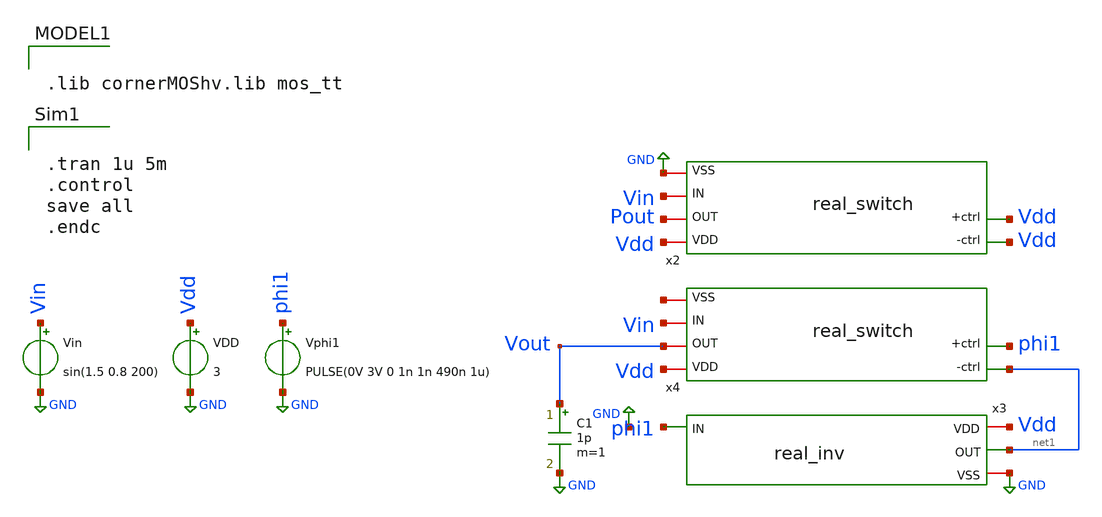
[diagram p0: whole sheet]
** sch_path: real_circuit/sandbox/TGATE_tb.sch
**.subckt TGATE_tb
VDD Vdd GND 3
Vin Vin GND sin(1.5 0.8 200)
Vphi1 phi1 GND PULSE(0V 3V 0 1n 1n 490n 1u)
x2 Vdd Vdd Pout Vin Vdd GND real_switch
x3 Vdd phi1 net1 GND real_inv
x4 net1 Vdd Vout Vin phi1 net2 real_switch
C1 Vout GND 1p m=1
**** begin user architecture code


.tran 1u 5m
.control
save all
.endc



.lib cornerMOShv.lib mos_tt

**** end user architecture code
**.ends

* expanding   symbol:  /foss/designs/real/real_switch.sym # of pins=6
** sym_path: real_circuit/sandbox/real_switch.sym
** sch_path: real_circuit/sandbox/real_switch.sch
.subckt real_switch -ctrl VDD OUT IN +ctrl VSS
*.iopin IN
*.iopin OUT
*.iopin VDD
*.iopin VSS
*.ipin +ctrl
*.ipin -ctrl
XM1 OUT -ctrl IN VSS sg13_hv_nmos w=1u l=0.6u ng=1 m=1 mm_ok=1
XM2 OUT +ctrl IN VDD sg13_hv_pmos w=2.5u l=0.6u ng=1 m=1 mm_ok=1
.ends


* expanding   symbol:  /foss/designs/real/real_inv.sym # of pins=4
** sym_path: real_circuit/real_inv.sym
** sch_path: real_circuit/real_inv.sch
.subckt real_inv VDD IN OUT VSS
*.iopin VDD
*.iopin VSS
*.ipin IN
*.opin OUT
XM1 OUT IN VDD VDD sg13_hv_pmos w=0.6u l=0.4u ng=1 m=1 mm_ok=1
XM2 OUT IN VSS VSS sg13_hv_nmos w=0.3u l=0.45u ng=1 m=1 mm_ok=1
.ends

.GLOBAL GND
.end
